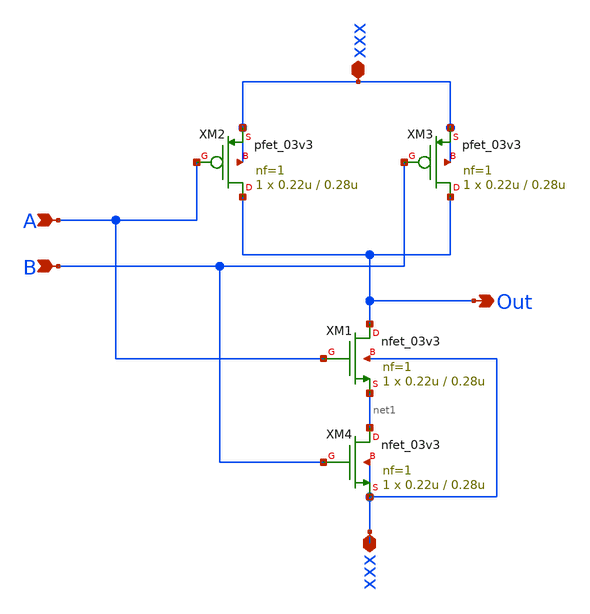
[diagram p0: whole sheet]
** sch_path: 2bit_Comparator/2x_drive/my_nand.sch
**.subckt my_nand A Out B xxx xxx
*.ipin A
*.opin Out
*.ipin B
*.iopin xxx
*.iopin xxx
XM1 Out A net1 xxx nfet_03v3 L=0.28u W=0.22u nf=1 ad='int((nf+1)/2) * W/nf * 0.18u' as='int((nf+2)/2) * W/nf * 0.18u'
+ pd='2*int((nf+1)/2) * (W/nf + 0.18u)' ps='2*int((nf+2)/2) * (W/nf + 0.18u)' nrd='0.18u / W' nrs='0.18u / W'
+ sa=0 sb=0 sd=0 m=1
XM2 Out A xxx xxx pfet_03v3 L=0.28u W=0.22u nf=1 ad='int((nf+1)/2) * W/nf * 0.18u' as='int((nf+2)/2) * W/nf * 0.18u'
+ pd='2*int((nf+1)/2) * (W/nf + 0.18u)' ps='2*int((nf+2)/2) * (W/nf + 0.18u)' nrd='0.18u / W' nrs='0.18u / W'
+ sa=0 sb=0 sd=0 m=1
XM3 Out B xxx xxx pfet_03v3 L=0.28u W=0.22u nf=1 ad='int((nf+1)/2) * W/nf * 0.18u' as='int((nf+2)/2) * W/nf * 0.18u'
+ pd='2*int((nf+1)/2) * (W/nf + 0.18u)' ps='2*int((nf+2)/2) * (W/nf + 0.18u)' nrd='0.18u / W' nrs='0.18u / W'
+ sa=0 sb=0 sd=0 m=1
XM4 net1 B xxx xxx nfet_03v3 L=0.28u W=0.22u nf=1 ad='int((nf+1)/2) * W/nf * 0.18u' as='int((nf+2)/2) * W/nf * 0.18u'
+ pd='2*int((nf+1)/2) * (W/nf + 0.18u)' ps='2*int((nf+2)/2) * (W/nf + 0.18u)' nrd='0.18u / W' nrs='0.18u / W'
+ sa=0 sb=0 sd=0 m=1
**.ends
.end
